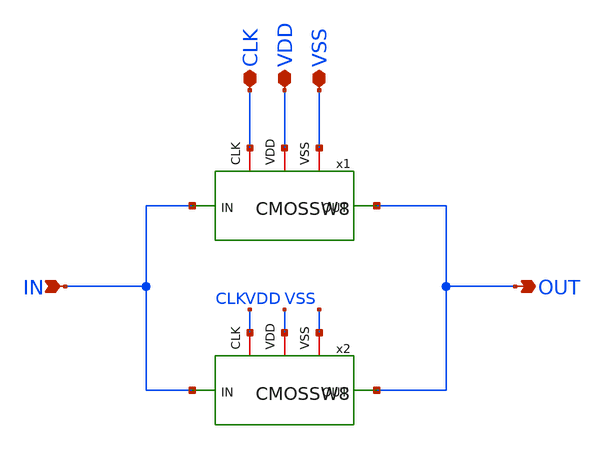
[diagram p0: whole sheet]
** sch_path: CMOSSW16.sch
**.subckt CMOSSW16 IN OUT VSS VDD CLK
*.ipin IN
*.opin OUT
*.iopin VSS
*.iopin VDD
*.iopin CLK
x1 CLK VSS OUT IN VDD CMOSSW8
x2 CLK VSS OUT IN VDD CMOSSW8
**.ends
.end
